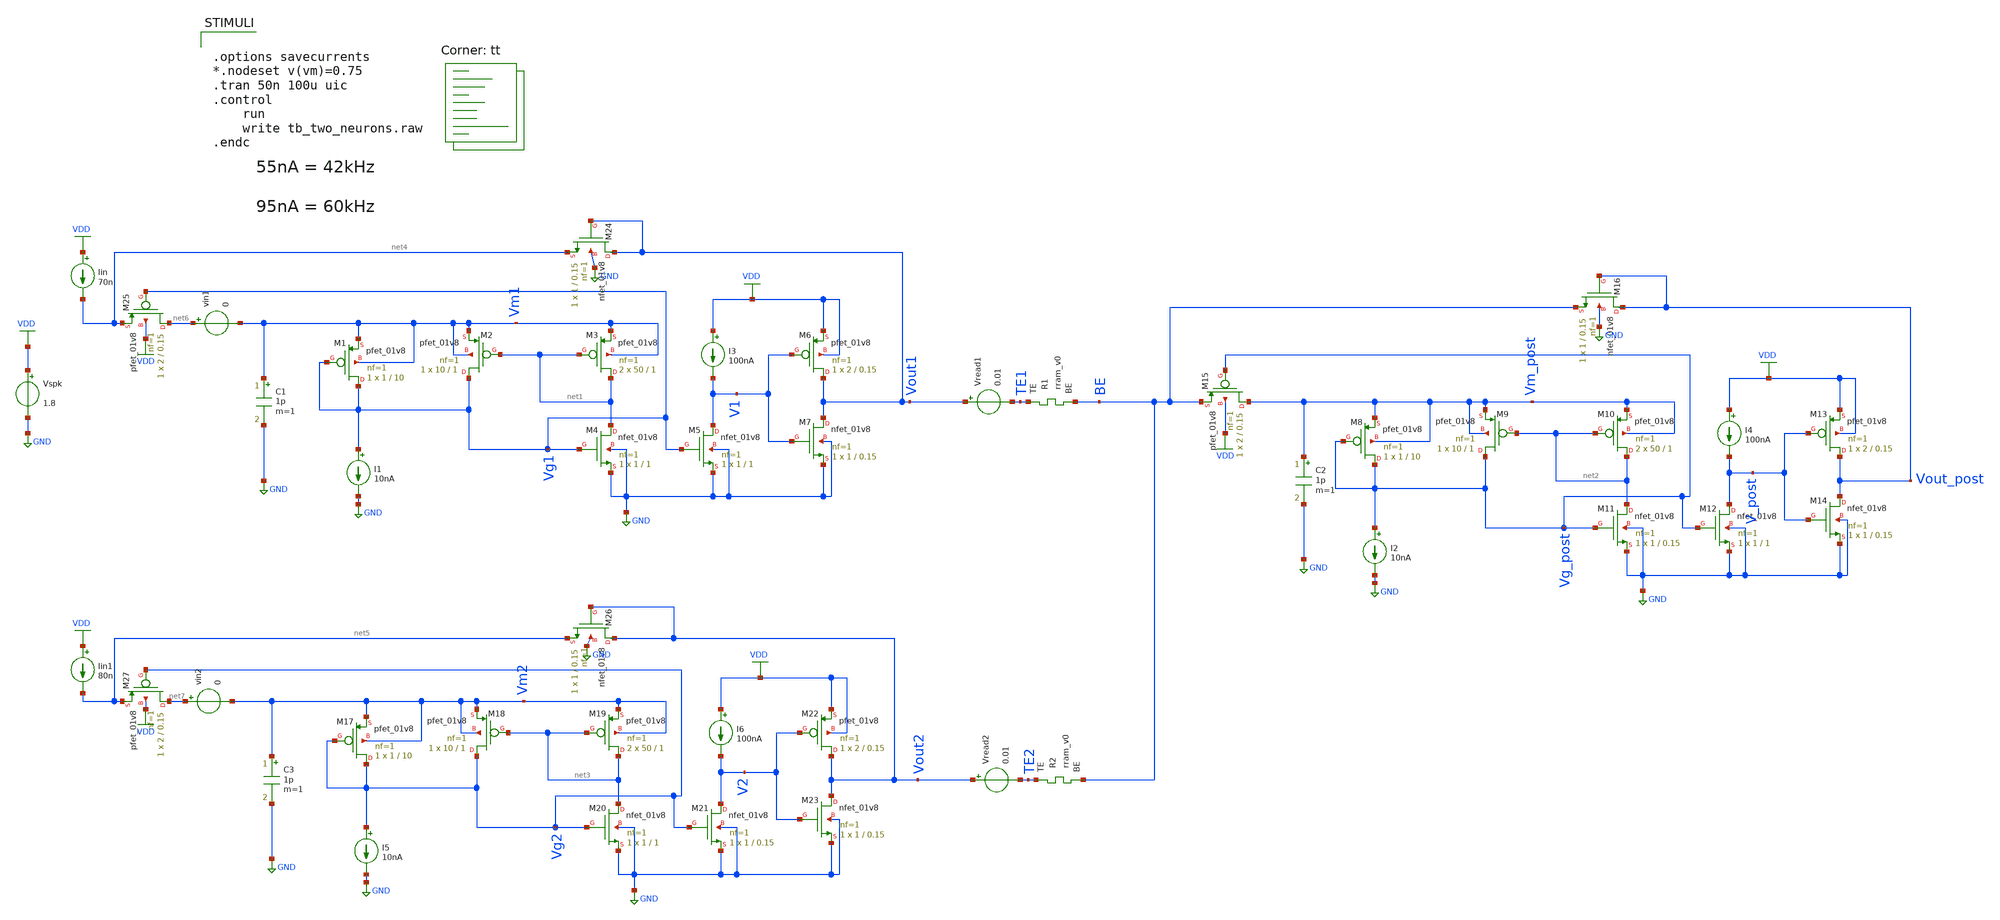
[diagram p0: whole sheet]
** sch_path: Neuron/ultralif/tb_two_neurons_conretro.sch
**.subckt tb_two_neurons_conretro
XM1 Vg1 Vg1 Vm1 Vm1 sky130_fd_pr__pfet_01v8 L=10 W=1 nf=1 ad='int((nf+1)/2) * W/nf * 0.29' as='int((nf+2)/2) * W/nf * 0.29'
+ pd='2*int((nf+1)/2) * (W/nf + 0.29)' ps='2*int((nf+2)/2) * (W/nf + 0.29)' nrd='0.29 / W' nrs='0.29 / W'
+ sa=0 sb=0 sd=0 mult=1 m=1
XM2 Vg1 net1 Vm1 Vm1 sky130_fd_pr__pfet_01v8 L=1 W=10 nf=1 ad='int((nf+1)/2) * W/nf * 0.29' as='int((nf+2)/2) * W/nf * 0.29'
+ pd='2*int((nf+1)/2) * (W/nf + 0.29)' ps='2*int((nf+2)/2) * (W/nf + 0.29)' nrd='0.29 / W' nrs='0.29 / W'
+ sa=0 sb=0 sd=0 mult=1 m=1
XM3 net1 net1 Vm1 Vm1 sky130_fd_pr__pfet_01v8 L=1 W=50 nf=1 ad='int((nf+1)/2) * W/nf * 0.29' as='int((nf+2)/2) * W/nf * 0.29'
+ pd='2*int((nf+1)/2) * (W/nf + 0.29)' ps='2*int((nf+2)/2) * (W/nf + 0.29)' nrd='0.29 / W' nrs='0.29 / W'
+ sa=0 sb=0 sd=0 mult=2 m=2
XM4 net1 Vg1 GND GND sky130_fd_pr__nfet_01v8 L=1 W=1 nf=1 ad='int((1 + 1)/2) * 1 / 1 * 0.29' as='int((1 + 2)/2) * 1 / 1 * 0.29'
+ pd='2*int((1 + 1)/2) * (1 / 1 + 0.29)' ps='2*int((1 + 2)/2) * (1 / 1 + 0.29)' nrd='0.29 / 1 ' nrs='0.29 / 1 '
+ sa=0 sb=0 sd=0 mult=1 m=1
XM5 V1 Vg1 GND GND sky130_fd_pr__nfet_01v8 L=1 W=1 nf=1 ad='int((1 + 1)/2) * 1 / 1 * 0.29' as='int((1 + 2)/2) * 1 / 1 * 0.29'
+ pd='2*int((1 + 1)/2) * (1 / 1 + 0.29)' ps='2*int((1 + 2)/2) * (1 / 1 + 0.29)' nrd='0.29 / 1 ' nrs='0.29 / 1 '
+ sa=0 sb=0 sd=0 mult=1 m=1
XM6 Vout1 V1 VDD VDD sky130_fd_pr__pfet_01v8 L=0.15 W=2 nf=1 ad='int((nf+1)/2) * W/nf * 0.29' as='int((nf+2)/2) * W/nf * 0.29'
+ pd='2*int((nf+1)/2) * (W/nf + 0.29)' ps='2*int((nf+2)/2) * (W/nf + 0.29)' nrd='0.29 / W' nrs='0.29 / W'
+ sa=0 sb=0 sd=0 mult=1 m=1
XM7 Vout1 V1 GND GND sky130_fd_pr__nfet_01v8 L=0.15 W=1 nf=1 ad='int((1 + 1)/2) * 1 / 1 * 0.29' as='int((1 + 2)/2) * 1 / 1 * 0.29'
+ pd='2*int((1 + 1)/2) * (1 / 1 + 0.29)' ps='2*int((1 + 2)/2) * (1 / 1 + 0.29)' nrd='0.29 / 1 ' nrs='0.29 / 1 '
+ sa=0 sb=0 sd=0 mult=1 m=1
I1 Vg1 GND 10nA
Vspk VDD GND 1.8
C1 Vm1 GND 1p m=1
Iin VDD net4 70n
I3 VDD V1 100nA
XR1 TE1 BE rram_v0
Vread1 Vout1 TE1 0.01
XM8 Vg_post Vg_post Vm_post Vm_post sky130_fd_pr__pfet_01v8 L=10 W=1 nf=1 ad='int((nf+1)/2) * W/nf * 0.29'
+ as='int((nf+2)/2) * W/nf * 0.29' pd='2*int((nf+1)/2) * (W/nf + 0.29)' ps='2*int((nf+2)/2) * (W/nf + 0.29)'
+ nrd='0.29 / W' nrs='0.29 / W' sa=0 sb=0 sd=0 mult=1 m=1
XM9 Vg_post net2 Vm_post Vm_post sky130_fd_pr__pfet_01v8 L=1 W=10 nf=1 ad='int((nf+1)/2) * W/nf * 0.29'
+ as='int((nf+2)/2) * W/nf * 0.29' pd='2*int((nf+1)/2) * (W/nf + 0.29)' ps='2*int((nf+2)/2) * (W/nf + 0.29)'
+ nrd='0.29 / W' nrs='0.29 / W' sa=0 sb=0 sd=0 mult=1 m=1
XM10 net2 net2 Vm_post Vm_post sky130_fd_pr__pfet_01v8 L=1 W=50 nf=1 ad='int((nf+1)/2) * W/nf * 0.29'
+ as='int((nf+2)/2) * W/nf * 0.29' pd='2*int((nf+1)/2) * (W/nf + 0.29)' ps='2*int((nf+2)/2) * (W/nf + 0.29)'
+ nrd='0.29 / W' nrs='0.29 / W' sa=0 sb=0 sd=0 mult=2 m=2
XM11 net2 Vg_post GND GND sky130_fd_pr__nfet_01v8 L=0.15 W=1 nf=1 ad='int((1 + 1)/2) * 1 / 1 * 0.29'
+ as='int((1 + 2)/2) * 1 / 1 * 0.29' pd='2*int((1 + 1)/2) * (1 / 1 + 0.29)' ps='2*int((1 + 2)/2) * (1 / 1 + 0.29)'
+ nrd='0.29 / 1 ' nrs='0.29 / 1 ' sa=0 sb=0 sd=0 mult=1 m=1
XM12 V_post Vg_post GND GND sky130_fd_pr__nfet_01v8 L=1 W=1 nf=1 ad='int((1 + 1)/2) * 1 / 1 * 0.29' as='int((1 + 2)/2) * 1 / 1 * 0.29'
+ pd='2*int((1 + 1)/2) * (1 / 1 + 0.29)' ps='2*int((1 + 2)/2) * (1 / 1 + 0.29)' nrd='0.29 / 1 ' nrs='0.29 / 1 '
+ sa=0 sb=0 sd=0 mult=1 m=1
XM13 Vout_post V_post VDD VDD sky130_fd_pr__pfet_01v8 L=0.15 W=2 nf=1 ad='int((nf+1)/2) * W/nf * 0.29'
+ as='int((nf+2)/2) * W/nf * 0.29' pd='2*int((nf+1)/2) * (W/nf + 0.29)' ps='2*int((nf+2)/2) * (W/nf + 0.29)'
+ nrd='0.29 / W' nrs='0.29 / W' sa=0 sb=0 sd=0 mult=1 m=1
XM14 Vout_post V_post GND GND sky130_fd_pr__nfet_01v8 L=0.15 W=1 nf=1 ad='int((1 + 1)/2) * 1 / 1 * 0.29'
+ as='int((1 + 2)/2) * 1 / 1 * 0.29' pd='2*int((1 + 1)/2) * (1 / 1 + 0.29)' ps='2*int((1 + 2)/2) * (1 / 1 + 0.29)'
+ nrd='0.29 / 1 ' nrs='0.29 / 1 ' sa=0 sb=0 sd=0 mult=1 m=1
I2 Vg_post GND 10nA
C2 Vm_post GND 1p m=1
I4 VDD V_post 100nA
XM15 Vm_post Vg_post BE VDD sky130_fd_pr__pfet_01v8 L=0.15 W=2 nf=1 ad='int((nf+1)/2) * W/nf * 0.29'
+ as='int((nf+2)/2) * W/nf * 0.29' pd='2*int((nf+1)/2) * (W/nf + 0.29)' ps='2*int((nf+2)/2) * (W/nf + 0.29)'
+ nrd='0.29 / W' nrs='0.29 / W' sa=0 sb=0 sd=0 mult=1 m=1
XM17 Vg2 Vg2 Vm2 Vm2 sky130_fd_pr__pfet_01v8 L=10 W=1 nf=1 ad='int((nf+1)/2) * W/nf * 0.29' as='int((nf+2)/2) * W/nf * 0.29'
+ pd='2*int((nf+1)/2) * (W/nf + 0.29)' ps='2*int((nf+2)/2) * (W/nf + 0.29)' nrd='0.29 / W' nrs='0.29 / W'
+ sa=0 sb=0 sd=0 mult=1 m=1
XM18 Vg2 net3 Vm2 Vm2 sky130_fd_pr__pfet_01v8 L=1 W=10 nf=1 ad='int((nf+1)/2) * W/nf * 0.29' as='int((nf+2)/2) * W/nf * 0.29'
+ pd='2*int((nf+1)/2) * (W/nf + 0.29)' ps='2*int((nf+2)/2) * (W/nf + 0.29)' nrd='0.29 / W' nrs='0.29 / W'
+ sa=0 sb=0 sd=0 mult=1 m=1
XM19 net3 net3 Vm2 Vm2 sky130_fd_pr__pfet_01v8 L=1 W=50 nf=1 ad='int((nf+1)/2) * W/nf * 0.29' as='int((nf+2)/2) * W/nf * 0.29'
+ pd='2*int((nf+1)/2) * (W/nf + 0.29)' ps='2*int((nf+2)/2) * (W/nf + 0.29)' nrd='0.29 / W' nrs='0.29 / W'
+ sa=0 sb=0 sd=0 mult=2 m=2
XM20 net3 Vg2 GND GND sky130_fd_pr__nfet_01v8 L=1 W=1 nf=1 ad='int((1 + 1)/2) * 1 / 1 * 0.29' as='int((1 + 2)/2) * 1 / 1 * 0.29'
+ pd='2*int((1 + 1)/2) * (1 / 1 + 0.29)' ps='2*int((1 + 2)/2) * (1 / 1 + 0.29)' nrd='0.29 / 1 ' nrs='0.29 / 1 '
+ sa=0 sb=0 sd=0 mult=1 m=1
XM21 V2 Vg2 GND GND sky130_fd_pr__nfet_01v8 L=0.15 W=1 nf=1 ad='int((1 + 1)/2) * 1 / 1 * 0.29' as='int((1 + 2)/2) * 1 / 1 * 0.29'
+ pd='2*int((1 + 1)/2) * (1 / 1 + 0.29)' ps='2*int((1 + 2)/2) * (1 / 1 + 0.29)' nrd='0.29 / 1 ' nrs='0.29 / 1 '
+ sa=0 sb=0 sd=0 mult=1 m=1
XM22 Vout2 V2 VDD VDD sky130_fd_pr__pfet_01v8 L=0.15 W=2 nf=1 ad='int((nf+1)/2) * W/nf * 0.29' as='int((nf+2)/2) * W/nf * 0.29'
+ pd='2*int((nf+1)/2) * (W/nf + 0.29)' ps='2*int((nf+2)/2) * (W/nf + 0.29)' nrd='0.29 / W' nrs='0.29 / W'
+ sa=0 sb=0 sd=0 mult=1 m=1
XM23 Vout2 V2 GND GND sky130_fd_pr__nfet_01v8 L=0.15 W=1 nf=1 ad='int((1 + 1)/2) * 1 / 1 * 0.29' as='int((1 + 2)/2) * 1 / 1 * 0.29'
+ pd='2*int((1 + 1)/2) * (1 / 1 + 0.29)' ps='2*int((1 + 2)/2) * (1 / 1 + 0.29)' nrd='0.29 / 1 ' nrs='0.29 / 1 '
+ sa=0 sb=0 sd=0 mult=1 m=1
I5 Vg2 GND 10nA
C3 Vm2 GND 1p m=1
Iin1 VDD net5 80n
I6 VDD V2 100nA
XR2 TE2 BE rram_v0
Vread2 Vout2 TE2 0.01
XM16 Vout_post Vout_post BE GND sky130_fd_pr__nfet_01v8 L=0.15 W=1 nf=1 ad='int((1 + 1)/2) * 1 / 1 * 0.29'
+ as='int((1 + 2)/2) * 1 / 1 * 0.29' pd='2*int((1 + 1)/2) * (1 / 1 + 0.29)' ps='2*int((1 + 2)/2) * (1 / 1 + 0.29)'
+ nrd='0.29 / 1 ' nrs='0.29 / 1 ' sa=0 sb=0 sd=0 mult=1 m=1
XM24 Vout1 Vout1 net4 GND sky130_fd_pr__nfet_01v8 L=0.15 W=1 nf=1 ad='int((1 + 1)/2) * 1 / 1 * 0.29'
+ as='int((1 + 2)/2) * 1 / 1 * 0.29' pd='2*int((1 + 1)/2) * (1 / 1 + 0.29)' ps='2*int((1 + 2)/2) * (1 / 1 + 0.29)'
+ nrd='0.29 / 1 ' nrs='0.29 / 1 ' sa=0 sb=0 sd=0 mult=1 m=1
XM25 net6 Vg1 net4 VDD sky130_fd_pr__pfet_01v8 L=0.15 W=2 nf=1 ad='int((nf+1)/2) * W/nf * 0.29' as='int((nf+2)/2) * W/nf * 0.29'
+ pd='2*int((nf+1)/2) * (W/nf + 0.29)' ps='2*int((nf+2)/2) * (W/nf + 0.29)' nrd='0.29 / W' nrs='0.29 / W'
+ sa=0 sb=0 sd=0 mult=1 m=1
XM26 Vout2 Vout2 net5 GND sky130_fd_pr__nfet_01v8 L=0.15 W=1 nf=1 ad='int((1 + 1)/2) * 1 / 1 * 0.29'
+ as='int((1 + 2)/2) * 1 / 1 * 0.29' pd='2*int((1 + 1)/2) * (1 / 1 + 0.29)' ps='2*int((1 + 2)/2) * (1 / 1 + 0.29)'
+ nrd='0.29 / 1 ' nrs='0.29 / 1 ' sa=0 sb=0 sd=0 mult=1 m=1
XM27 net7 Vg2 net5 VDD sky130_fd_pr__pfet_01v8 L=0.15 W=2 nf=1 ad='int((nf+1)/2) * W/nf * 0.29' as='int((nf+2)/2) * W/nf * 0.29'
+ pd='2*int((nf+1)/2) * (W/nf + 0.29)' ps='2*int((nf+2)/2) * (W/nf + 0.29)' nrd='0.29 / W' nrs='0.29 / W'
+ sa=0 sb=0 sd=0 mult=1 m=1
vin1 net6 Vm1 0
vin2 net7 Vm2 0
**** begin user architecture code
.lib $::SKYWATER_MODELS/sky130.lib.spice tt

** opencircuitdesign pdks install
.inc $::SKYWATER_MODELS/rram_v0.spice

**** end user architecture code
**.ends
.GLOBAL GND
.GLOBAL VDD
**** begin user architecture code


.options savecurrents
*.nodeset v(vm)=0.75
.tran 50n 100u uic
.control
	run
	write tb_two_neurons.raw
.endc


**** end user architecture code
.end
